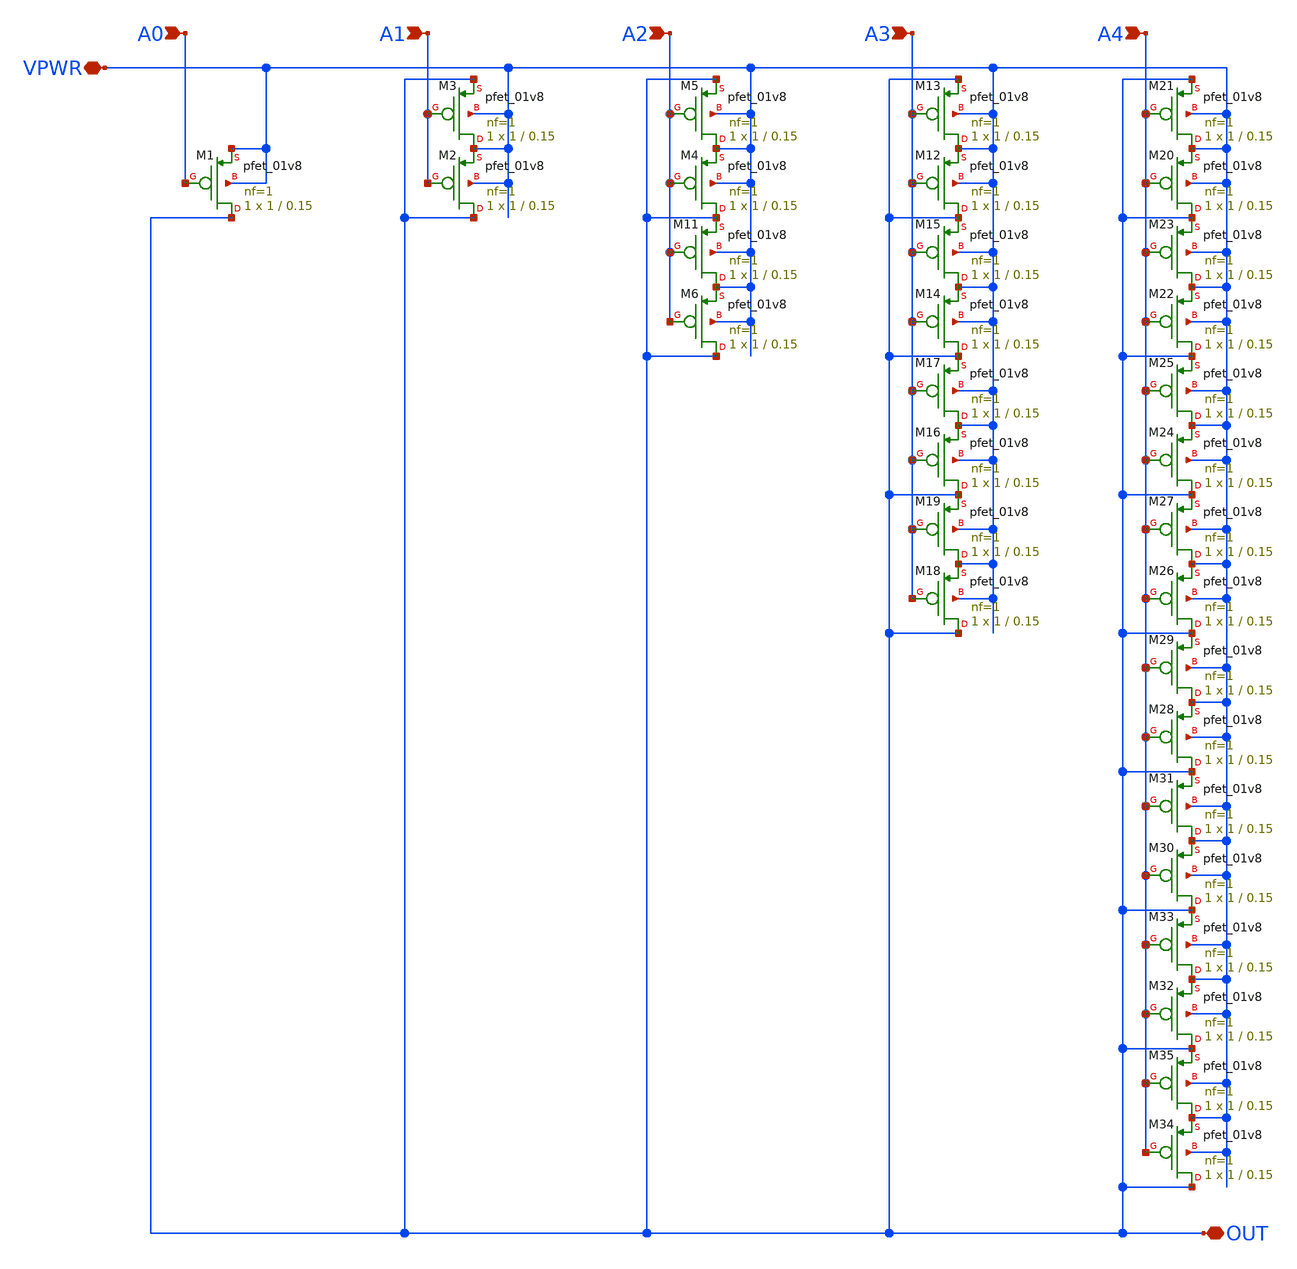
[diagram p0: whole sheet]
** sch_path: libs.ref/sky130_hilas_sc/xschem/sky130_hilas_DAC5bit01.sch
**.subckt sky130_hilas_DAC5bit01 VPWR A4 OUT A3 A2 A1 A0
*.iopin VPWR
*.ipin A4
*.iopin OUT
*.ipin A3
*.ipin A2
*.ipin A1
*.ipin A0
XM1 OUT A0 VPWR VPWR sky130_fd_pr__pfet_01v8 L=0.15 W=1 nf=1 ad='int((nf+1)/2) * W/nf * 0.29' as='int((nf+2)/2) * W/nf * 0.29'
+ pd='2*int((nf+1)/2) * (W/nf + 0.29)' ps='2*int((nf+2)/2) * (W/nf + 0.29)' nrd='0.29 / W' nrs='0.29 / W'
+ sa=0 sb=0 sd=0 mult=1 m=1
XM2 OUT A1 VPWR VPWR sky130_fd_pr__pfet_01v8 L=0.15 W=1 nf=1 ad='int((nf+1)/2) * W/nf * 0.29' as='int((nf+2)/2) * W/nf * 0.29'
+ pd='2*int((nf+1)/2) * (W/nf + 0.29)' ps='2*int((nf+2)/2) * (W/nf + 0.29)' nrd='0.29 / W' nrs='0.29 / W'
+ sa=0 sb=0 sd=0 mult=1 m=1
XM3 VPWR A1 OUT VPWR sky130_fd_pr__pfet_01v8 L=0.15 W=1 nf=1 ad='int((nf+1)/2) * W/nf * 0.29' as='int((nf+2)/2) * W/nf * 0.29'
+ pd='2*int((nf+1)/2) * (W/nf + 0.29)' ps='2*int((nf+2)/2) * (W/nf + 0.29)' nrd='0.29 / W' nrs='0.29 / W'
+ sa=0 sb=0 sd=0 mult=1 m=1
XM4 OUT A2 VPWR VPWR sky130_fd_pr__pfet_01v8 L=0.15 W=1 nf=1 ad='int((nf+1)/2) * W/nf * 0.29' as='int((nf+2)/2) * W/nf * 0.29'
+ pd='2*int((nf+1)/2) * (W/nf + 0.29)' ps='2*int((nf+2)/2) * (W/nf + 0.29)' nrd='0.29 / W' nrs='0.29 / W'
+ sa=0 sb=0 sd=0 mult=1 m=1
XM5 VPWR A2 OUT VPWR sky130_fd_pr__pfet_01v8 L=0.15 W=1 nf=1 ad='int((nf+1)/2) * W/nf * 0.29' as='int((nf+2)/2) * W/nf * 0.29'
+ pd='2*int((nf+1)/2) * (W/nf + 0.29)' ps='2*int((nf+2)/2) * (W/nf + 0.29)' nrd='0.29 / W' nrs='0.29 / W'
+ sa=0 sb=0 sd=0 mult=1 m=1
XM6 OUT A2 VPWR VPWR sky130_fd_pr__pfet_01v8 L=0.15 W=1 nf=1 ad='int((nf+1)/2) * W/nf * 0.29' as='int((nf+2)/2) * W/nf * 0.29'
+ pd='2*int((nf+1)/2) * (W/nf + 0.29)' ps='2*int((nf+2)/2) * (W/nf + 0.29)' nrd='0.29 / W' nrs='0.29 / W'
+ sa=0 sb=0 sd=0 mult=1 m=1
XM11 VPWR A2 OUT VPWR sky130_fd_pr__pfet_01v8 L=0.15 W=1 nf=1 ad='int((nf+1)/2) * W/nf * 0.29' as='int((nf+2)/2) * W/nf * 0.29'
+ pd='2*int((nf+1)/2) * (W/nf + 0.29)' ps='2*int((nf+2)/2) * (W/nf + 0.29)' nrd='0.29 / W' nrs='0.29 / W'
+ sa=0 sb=0 sd=0 mult=1 m=1
XM12 OUT A3 VPWR VPWR sky130_fd_pr__pfet_01v8 L=0.15 W=1 nf=1 ad='int((nf+1)/2) * W/nf * 0.29' as='int((nf+2)/2) * W/nf * 0.29'
+ pd='2*int((nf+1)/2) * (W/nf + 0.29)' ps='2*int((nf+2)/2) * (W/nf + 0.29)' nrd='0.29 / W' nrs='0.29 / W'
+ sa=0 sb=0 sd=0 mult=1 m=1
XM13 VPWR A3 OUT VPWR sky130_fd_pr__pfet_01v8 L=0.15 W=1 nf=1 ad='int((nf+1)/2) * W/nf * 0.29' as='int((nf+2)/2) * W/nf * 0.29'
+ pd='2*int((nf+1)/2) * (W/nf + 0.29)' ps='2*int((nf+2)/2) * (W/nf + 0.29)' nrd='0.29 / W' nrs='0.29 / W'
+ sa=0 sb=0 sd=0 mult=1 m=1
XM14 OUT A3 VPWR VPWR sky130_fd_pr__pfet_01v8 L=0.15 W=1 nf=1 ad='int((nf+1)/2) * W/nf * 0.29' as='int((nf+2)/2) * W/nf * 0.29'
+ pd='2*int((nf+1)/2) * (W/nf + 0.29)' ps='2*int((nf+2)/2) * (W/nf + 0.29)' nrd='0.29 / W' nrs='0.29 / W'
+ sa=0 sb=0 sd=0 mult=1 m=1
XM15 VPWR A3 OUT VPWR sky130_fd_pr__pfet_01v8 L=0.15 W=1 nf=1 ad='int((nf+1)/2) * W/nf * 0.29' as='int((nf+2)/2) * W/nf * 0.29'
+ pd='2*int((nf+1)/2) * (W/nf + 0.29)' ps='2*int((nf+2)/2) * (W/nf + 0.29)' nrd='0.29 / W' nrs='0.29 / W'
+ sa=0 sb=0 sd=0 mult=1 m=1
XM16 OUT A3 VPWR VPWR sky130_fd_pr__pfet_01v8 L=0.15 W=1 nf=1 ad='int((nf+1)/2) * W/nf * 0.29' as='int((nf+2)/2) * W/nf * 0.29'
+ pd='2*int((nf+1)/2) * (W/nf + 0.29)' ps='2*int((nf+2)/2) * (W/nf + 0.29)' nrd='0.29 / W' nrs='0.29 / W'
+ sa=0 sb=0 sd=0 mult=1 m=1
XM17 VPWR A3 OUT VPWR sky130_fd_pr__pfet_01v8 L=0.15 W=1 nf=1 ad='int((nf+1)/2) * W/nf * 0.29' as='int((nf+2)/2) * W/nf * 0.29'
+ pd='2*int((nf+1)/2) * (W/nf + 0.29)' ps='2*int((nf+2)/2) * (W/nf + 0.29)' nrd='0.29 / W' nrs='0.29 / W'
+ sa=0 sb=0 sd=0 mult=1 m=1
XM18 OUT A3 VPWR VPWR sky130_fd_pr__pfet_01v8 L=0.15 W=1 nf=1 ad='int((nf+1)/2) * W/nf * 0.29' as='int((nf+2)/2) * W/nf * 0.29'
+ pd='2*int((nf+1)/2) * (W/nf + 0.29)' ps='2*int((nf+2)/2) * (W/nf + 0.29)' nrd='0.29 / W' nrs='0.29 / W'
+ sa=0 sb=0 sd=0 mult=1 m=1
XM19 VPWR A3 OUT VPWR sky130_fd_pr__pfet_01v8 L=0.15 W=1 nf=1 ad='int((nf+1)/2) * W/nf * 0.29' as='int((nf+2)/2) * W/nf * 0.29'
+ pd='2*int((nf+1)/2) * (W/nf + 0.29)' ps='2*int((nf+2)/2) * (W/nf + 0.29)' nrd='0.29 / W' nrs='0.29 / W'
+ sa=0 sb=0 sd=0 mult=1 m=1
XM20 OUT A4 VPWR VPWR sky130_fd_pr__pfet_01v8 L=0.15 W=1 nf=1 ad='int((nf+1)/2) * W/nf * 0.29' as='int((nf+2)/2) * W/nf * 0.29'
+ pd='2*int((nf+1)/2) * (W/nf + 0.29)' ps='2*int((nf+2)/2) * (W/nf + 0.29)' nrd='0.29 / W' nrs='0.29 / W'
+ sa=0 sb=0 sd=0 mult=1 m=1
XM21 VPWR A4 OUT VPWR sky130_fd_pr__pfet_01v8 L=0.15 W=1 nf=1 ad='int((nf+1)/2) * W/nf * 0.29' as='int((nf+2)/2) * W/nf * 0.29'
+ pd='2*int((nf+1)/2) * (W/nf + 0.29)' ps='2*int((nf+2)/2) * (W/nf + 0.29)' nrd='0.29 / W' nrs='0.29 / W'
+ sa=0 sb=0 sd=0 mult=1 m=1
XM22 OUT A4 VPWR VPWR sky130_fd_pr__pfet_01v8 L=0.15 W=1 nf=1 ad='int((nf+1)/2) * W/nf * 0.29' as='int((nf+2)/2) * W/nf * 0.29'
+ pd='2*int((nf+1)/2) * (W/nf + 0.29)' ps='2*int((nf+2)/2) * (W/nf + 0.29)' nrd='0.29 / W' nrs='0.29 / W'
+ sa=0 sb=0 sd=0 mult=1 m=1
XM23 VPWR A4 OUT VPWR sky130_fd_pr__pfet_01v8 L=0.15 W=1 nf=1 ad='int((nf+1)/2) * W/nf * 0.29' as='int((nf+2)/2) * W/nf * 0.29'
+ pd='2*int((nf+1)/2) * (W/nf + 0.29)' ps='2*int((nf+2)/2) * (W/nf + 0.29)' nrd='0.29 / W' nrs='0.29 / W'
+ sa=0 sb=0 sd=0 mult=1 m=1
XM24 OUT A4 VPWR VPWR sky130_fd_pr__pfet_01v8 L=0.15 W=1 nf=1 ad='int((nf+1)/2) * W/nf * 0.29' as='int((nf+2)/2) * W/nf * 0.29'
+ pd='2*int((nf+1)/2) * (W/nf + 0.29)' ps='2*int((nf+2)/2) * (W/nf + 0.29)' nrd='0.29 / W' nrs='0.29 / W'
+ sa=0 sb=0 sd=0 mult=1 m=1
XM25 VPWR A4 OUT VPWR sky130_fd_pr__pfet_01v8 L=0.15 W=1 nf=1 ad='int((nf+1)/2) * W/nf * 0.29' as='int((nf+2)/2) * W/nf * 0.29'
+ pd='2*int((nf+1)/2) * (W/nf + 0.29)' ps='2*int((nf+2)/2) * (W/nf + 0.29)' nrd='0.29 / W' nrs='0.29 / W'
+ sa=0 sb=0 sd=0 mult=1 m=1
XM26 OUT A4 VPWR VPWR sky130_fd_pr__pfet_01v8 L=0.15 W=1 nf=1 ad='int((nf+1)/2) * W/nf * 0.29' as='int((nf+2)/2) * W/nf * 0.29'
+ pd='2*int((nf+1)/2) * (W/nf + 0.29)' ps='2*int((nf+2)/2) * (W/nf + 0.29)' nrd='0.29 / W' nrs='0.29 / W'
+ sa=0 sb=0 sd=0 mult=1 m=1
XM27 VPWR A4 OUT VPWR sky130_fd_pr__pfet_01v8 L=0.15 W=1 nf=1 ad='int((nf+1)/2) * W/nf * 0.29' as='int((nf+2)/2) * W/nf * 0.29'
+ pd='2*int((nf+1)/2) * (W/nf + 0.29)' ps='2*int((nf+2)/2) * (W/nf + 0.29)' nrd='0.29 / W' nrs='0.29 / W'
+ sa=0 sb=0 sd=0 mult=1 m=1
XM28 OUT A4 VPWR VPWR sky130_fd_pr__pfet_01v8 L=0.15 W=1 nf=1 ad='int((nf+1)/2) * W/nf * 0.29' as='int((nf+2)/2) * W/nf * 0.29'
+ pd='2*int((nf+1)/2) * (W/nf + 0.29)' ps='2*int((nf+2)/2) * (W/nf + 0.29)' nrd='0.29 / W' nrs='0.29 / W'
+ sa=0 sb=0 sd=0 mult=1 m=1
XM29 VPWR A4 OUT VPWR sky130_fd_pr__pfet_01v8 L=0.15 W=1 nf=1 ad='int((nf+1)/2) * W/nf * 0.29' as='int((nf+2)/2) * W/nf * 0.29'
+ pd='2*int((nf+1)/2) * (W/nf + 0.29)' ps='2*int((nf+2)/2) * (W/nf + 0.29)' nrd='0.29 / W' nrs='0.29 / W'
+ sa=0 sb=0 sd=0 mult=1 m=1
XM30 OUT A4 VPWR VPWR sky130_fd_pr__pfet_01v8 L=0.15 W=1 nf=1 ad='int((nf+1)/2) * W/nf * 0.29' as='int((nf+2)/2) * W/nf * 0.29'
+ pd='2*int((nf+1)/2) * (W/nf + 0.29)' ps='2*int((nf+2)/2) * (W/nf + 0.29)' nrd='0.29 / W' nrs='0.29 / W'
+ sa=0 sb=0 sd=0 mult=1 m=1
XM31 VPWR A4 OUT VPWR sky130_fd_pr__pfet_01v8 L=0.15 W=1 nf=1 ad='int((nf+1)/2) * W/nf * 0.29' as='int((nf+2)/2) * W/nf * 0.29'
+ pd='2*int((nf+1)/2) * (W/nf + 0.29)' ps='2*int((nf+2)/2) * (W/nf + 0.29)' nrd='0.29 / W' nrs='0.29 / W'
+ sa=0 sb=0 sd=0 mult=1 m=1
XM32 OUT A4 VPWR VPWR sky130_fd_pr__pfet_01v8 L=0.15 W=1 nf=1 ad='int((nf+1)/2) * W/nf * 0.29' as='int((nf+2)/2) * W/nf * 0.29'
+ pd='2*int((nf+1)/2) * (W/nf + 0.29)' ps='2*int((nf+2)/2) * (W/nf + 0.29)' nrd='0.29 / W' nrs='0.29 / W'
+ sa=0 sb=0 sd=0 mult=1 m=1
XM33 VPWR A4 OUT VPWR sky130_fd_pr__pfet_01v8 L=0.15 W=1 nf=1 ad='int((nf+1)/2) * W/nf * 0.29' as='int((nf+2)/2) * W/nf * 0.29'
+ pd='2*int((nf+1)/2) * (W/nf + 0.29)' ps='2*int((nf+2)/2) * (W/nf + 0.29)' nrd='0.29 / W' nrs='0.29 / W'
+ sa=0 sb=0 sd=0 mult=1 m=1
XM34 OUT A4 VPWR VPWR sky130_fd_pr__pfet_01v8 L=0.15 W=1 nf=1 ad='int((nf+1)/2) * W/nf * 0.29' as='int((nf+2)/2) * W/nf * 0.29'
+ pd='2*int((nf+1)/2) * (W/nf + 0.29)' ps='2*int((nf+2)/2) * (W/nf + 0.29)' nrd='0.29 / W' nrs='0.29 / W'
+ sa=0 sb=0 sd=0 mult=1 m=1
XM35 VPWR A4 OUT VPWR sky130_fd_pr__pfet_01v8 L=0.15 W=1 nf=1 ad='int((nf+1)/2) * W/nf * 0.29' as='int((nf+2)/2) * W/nf * 0.29'
+ pd='2*int((nf+1)/2) * (W/nf + 0.29)' ps='2*int((nf+2)/2) * (W/nf + 0.29)' nrd='0.29 / W' nrs='0.29 / W'
+ sa=0 sb=0 sd=0 mult=1 m=1
**.ends
.end
